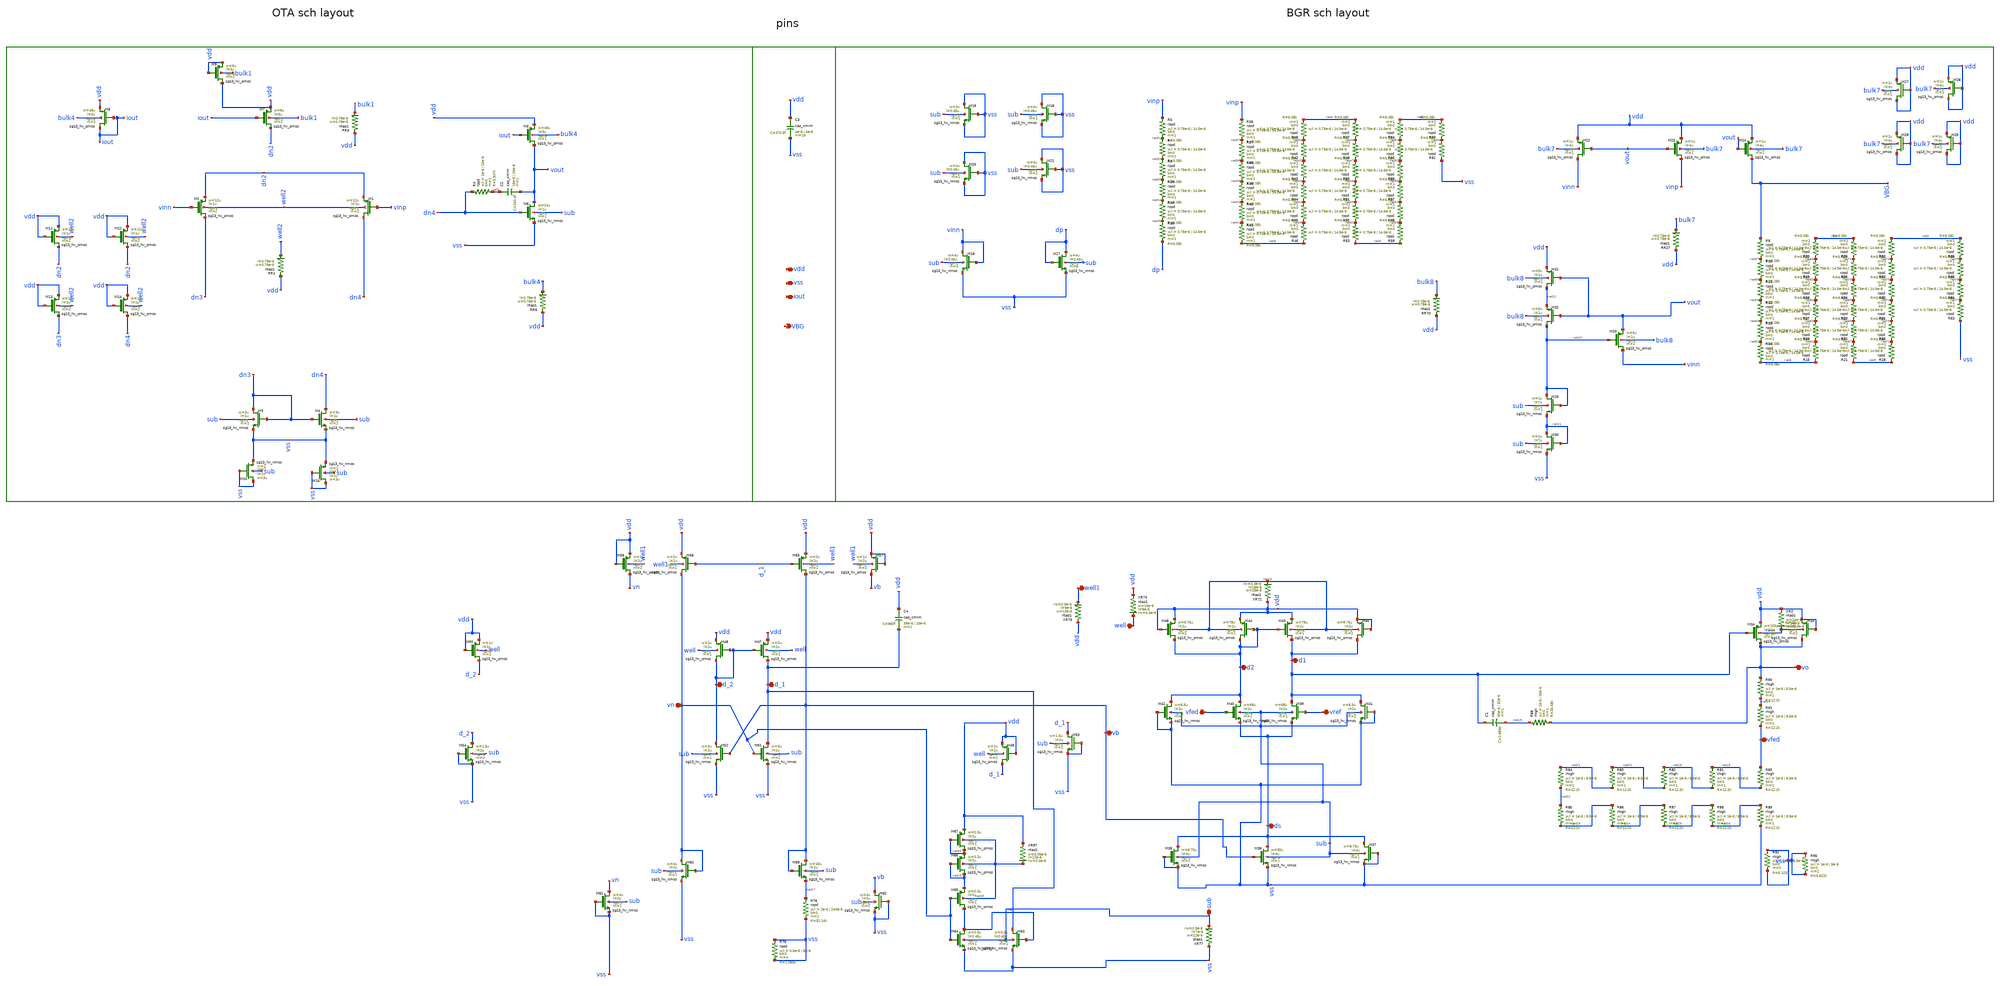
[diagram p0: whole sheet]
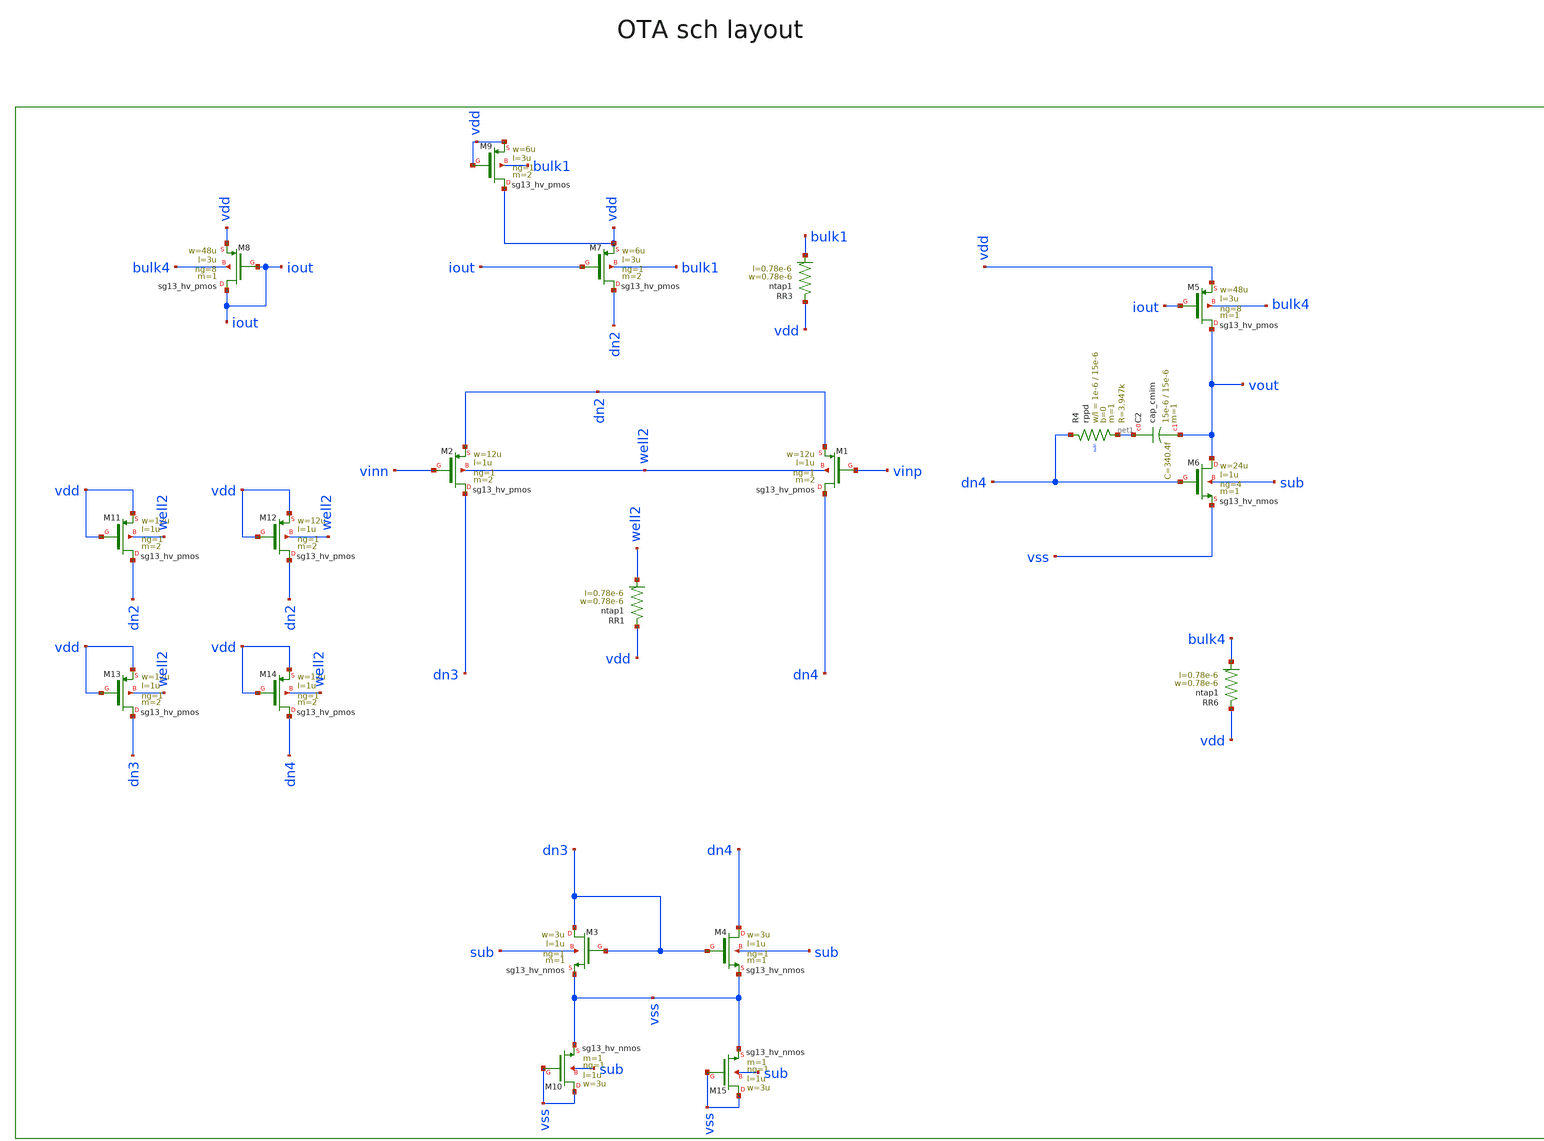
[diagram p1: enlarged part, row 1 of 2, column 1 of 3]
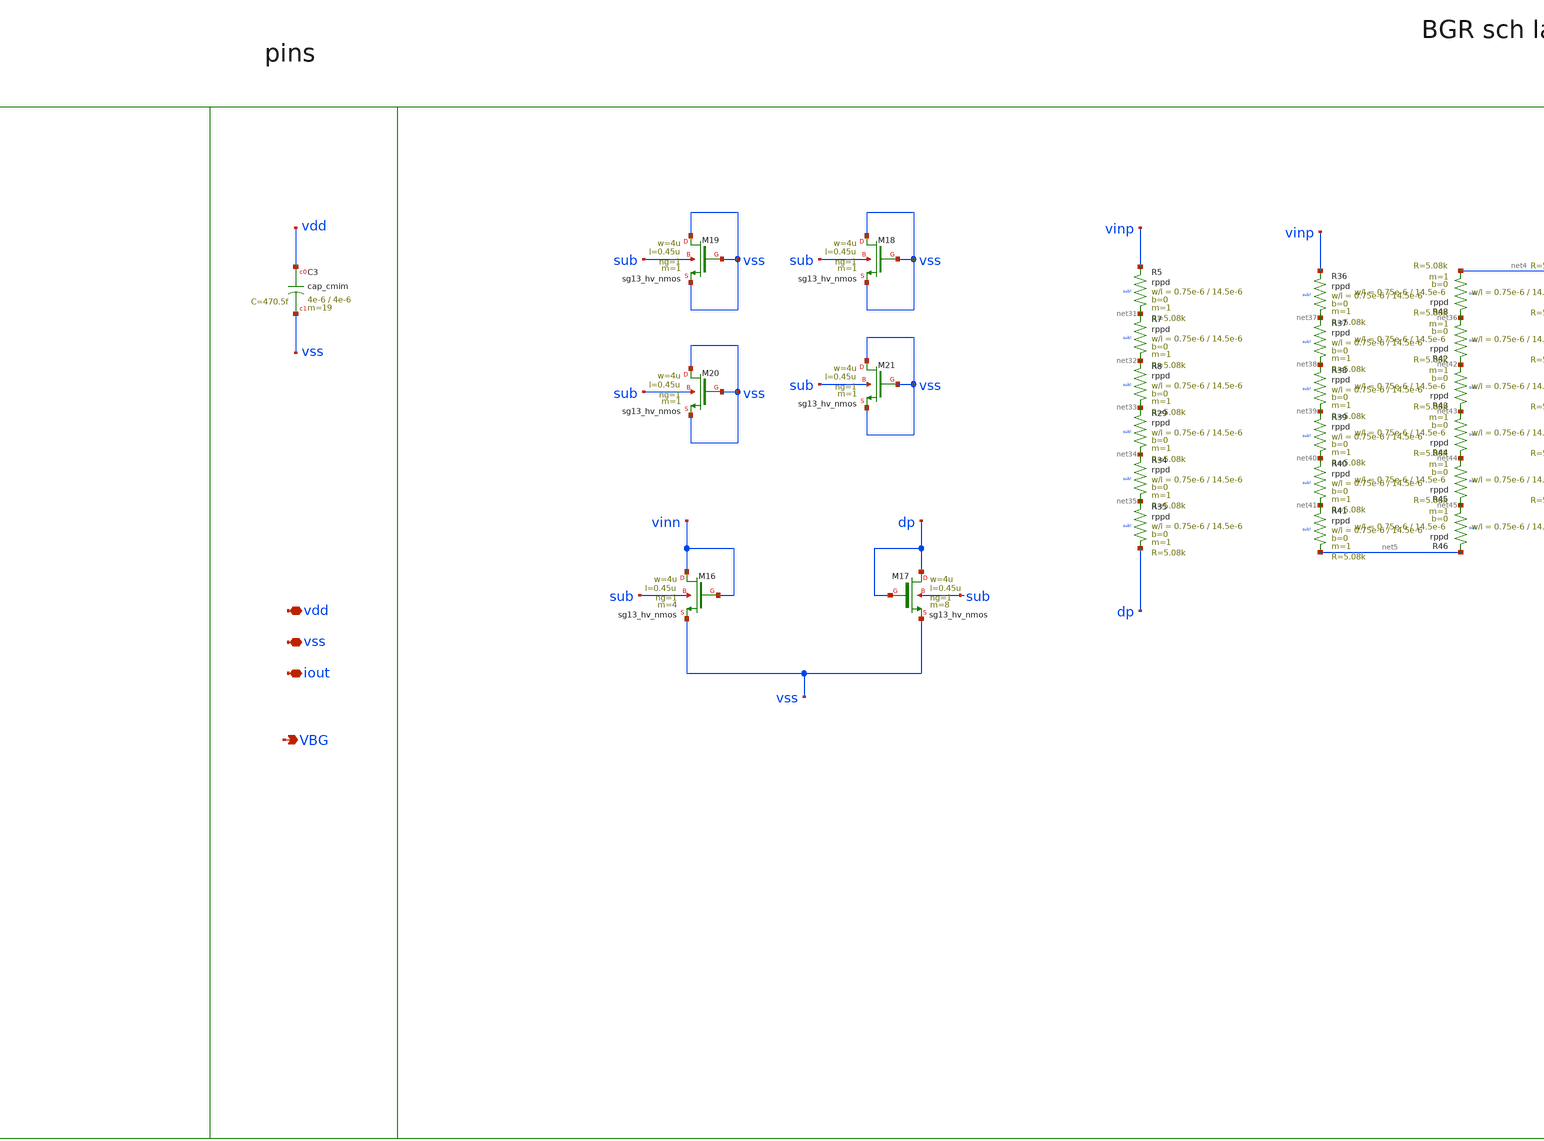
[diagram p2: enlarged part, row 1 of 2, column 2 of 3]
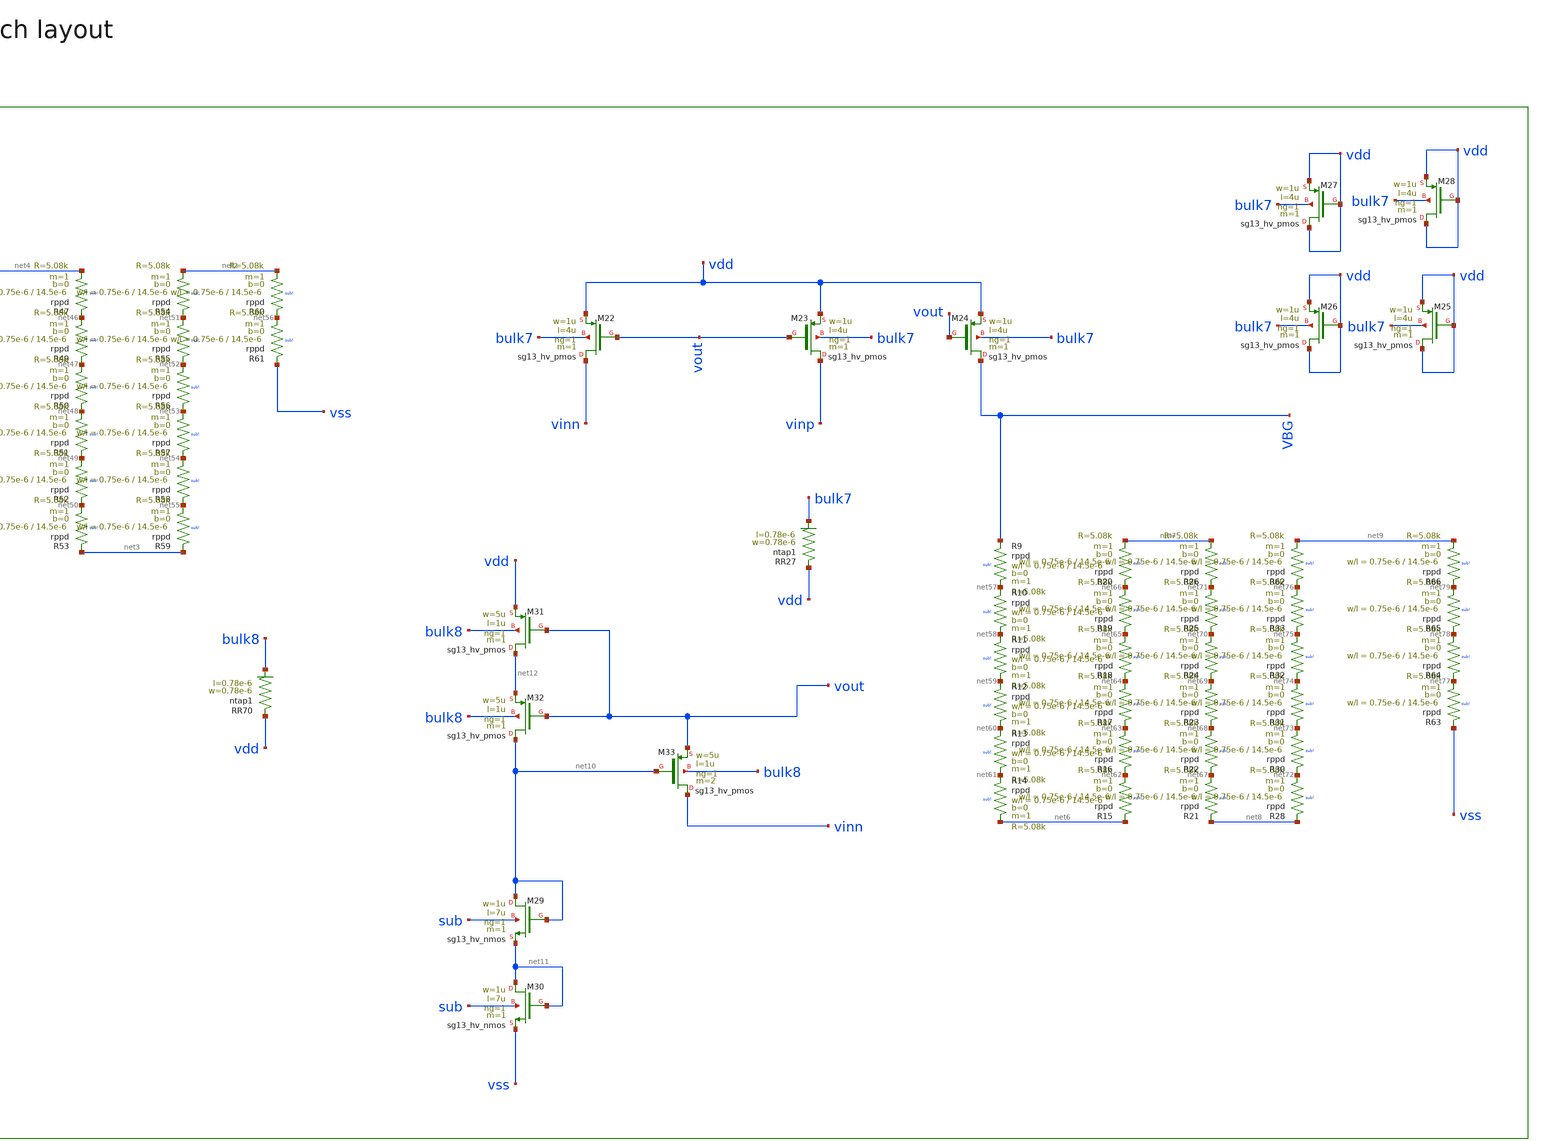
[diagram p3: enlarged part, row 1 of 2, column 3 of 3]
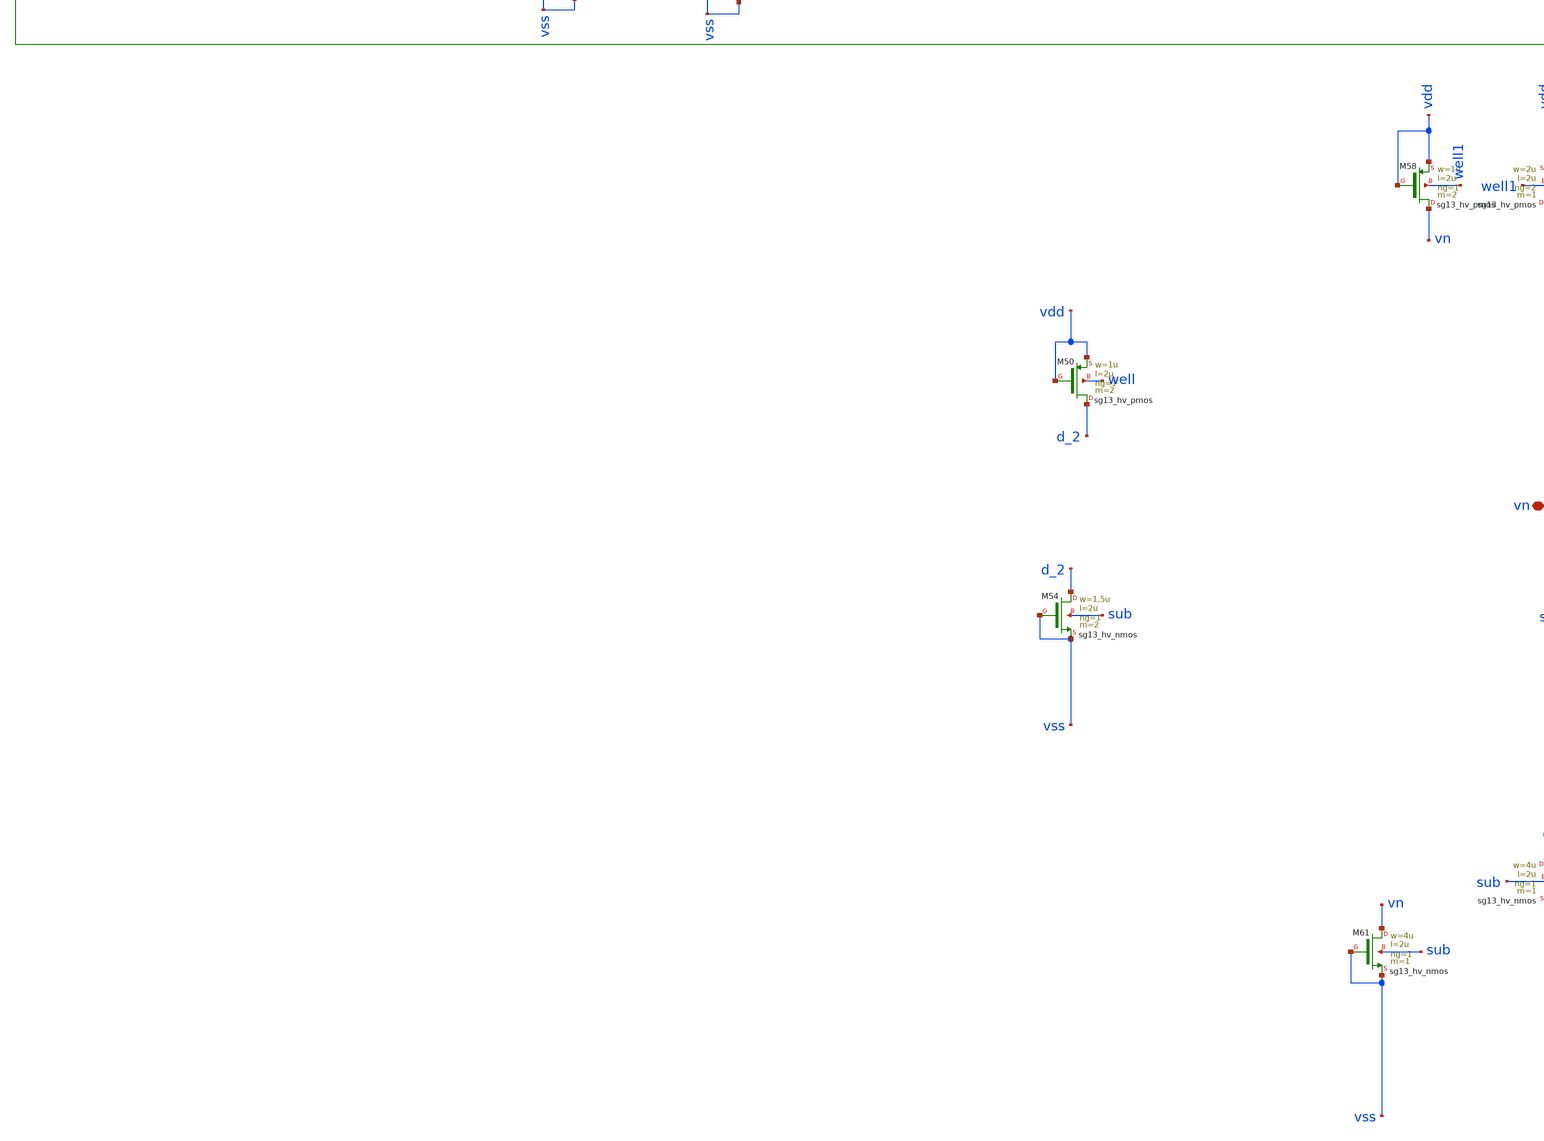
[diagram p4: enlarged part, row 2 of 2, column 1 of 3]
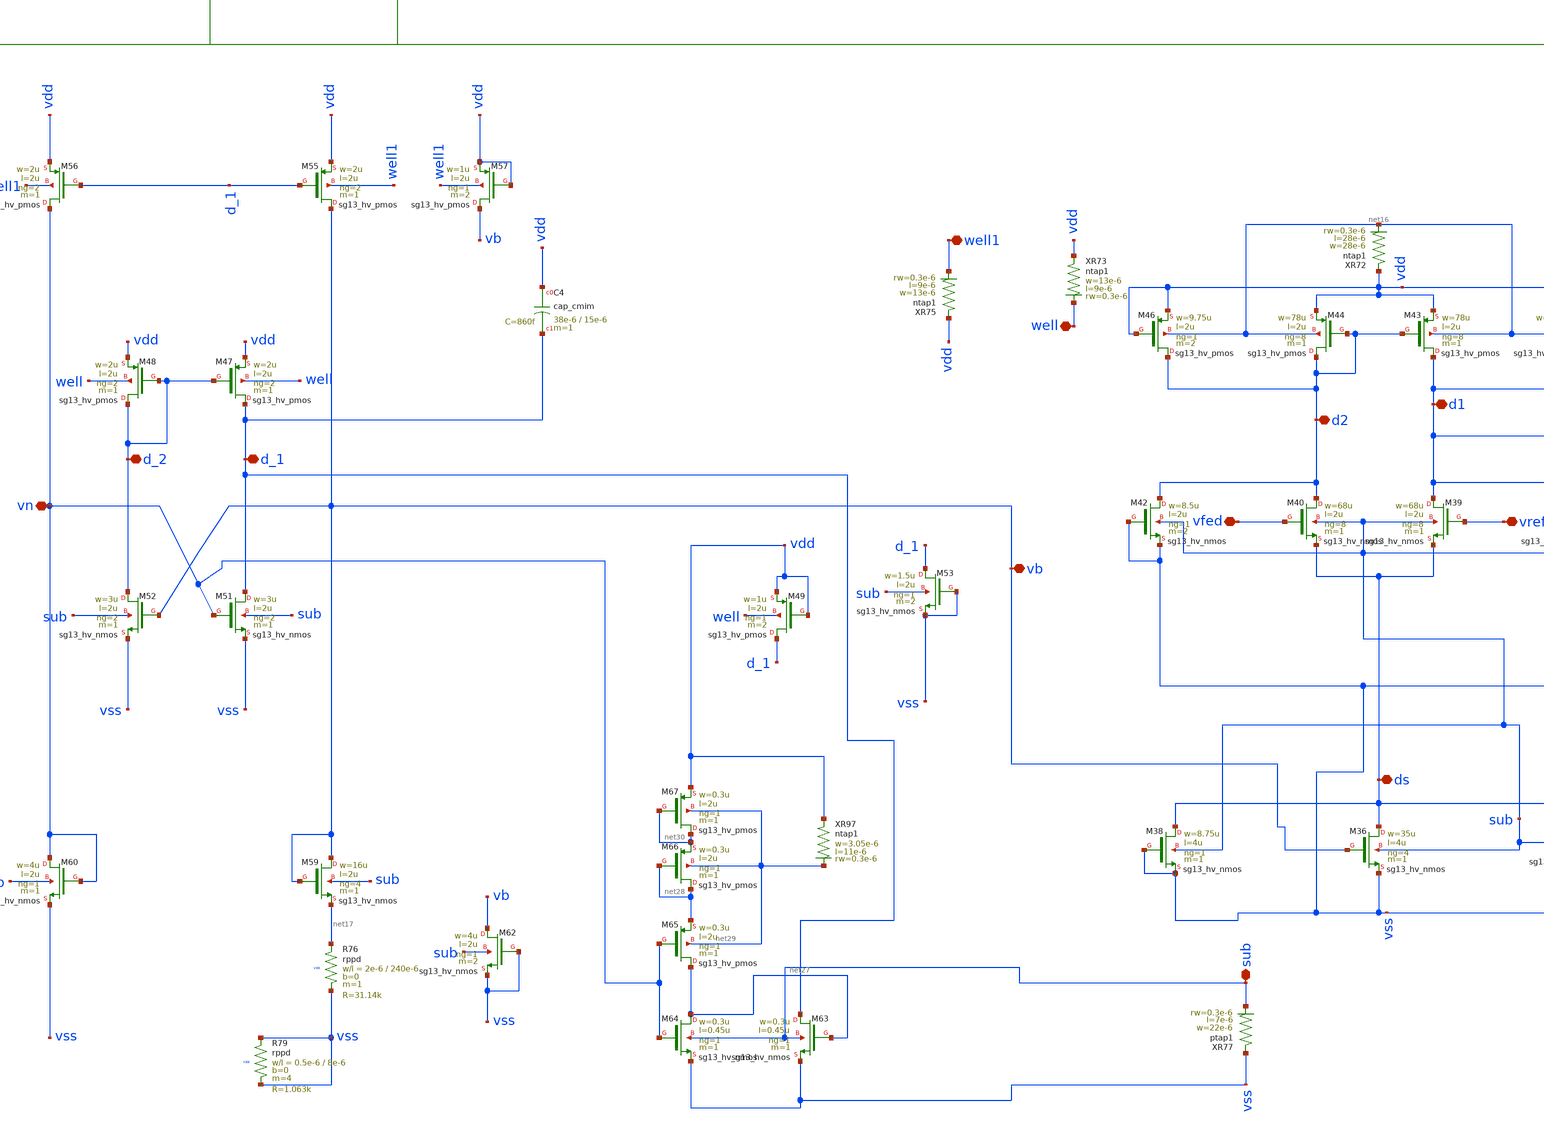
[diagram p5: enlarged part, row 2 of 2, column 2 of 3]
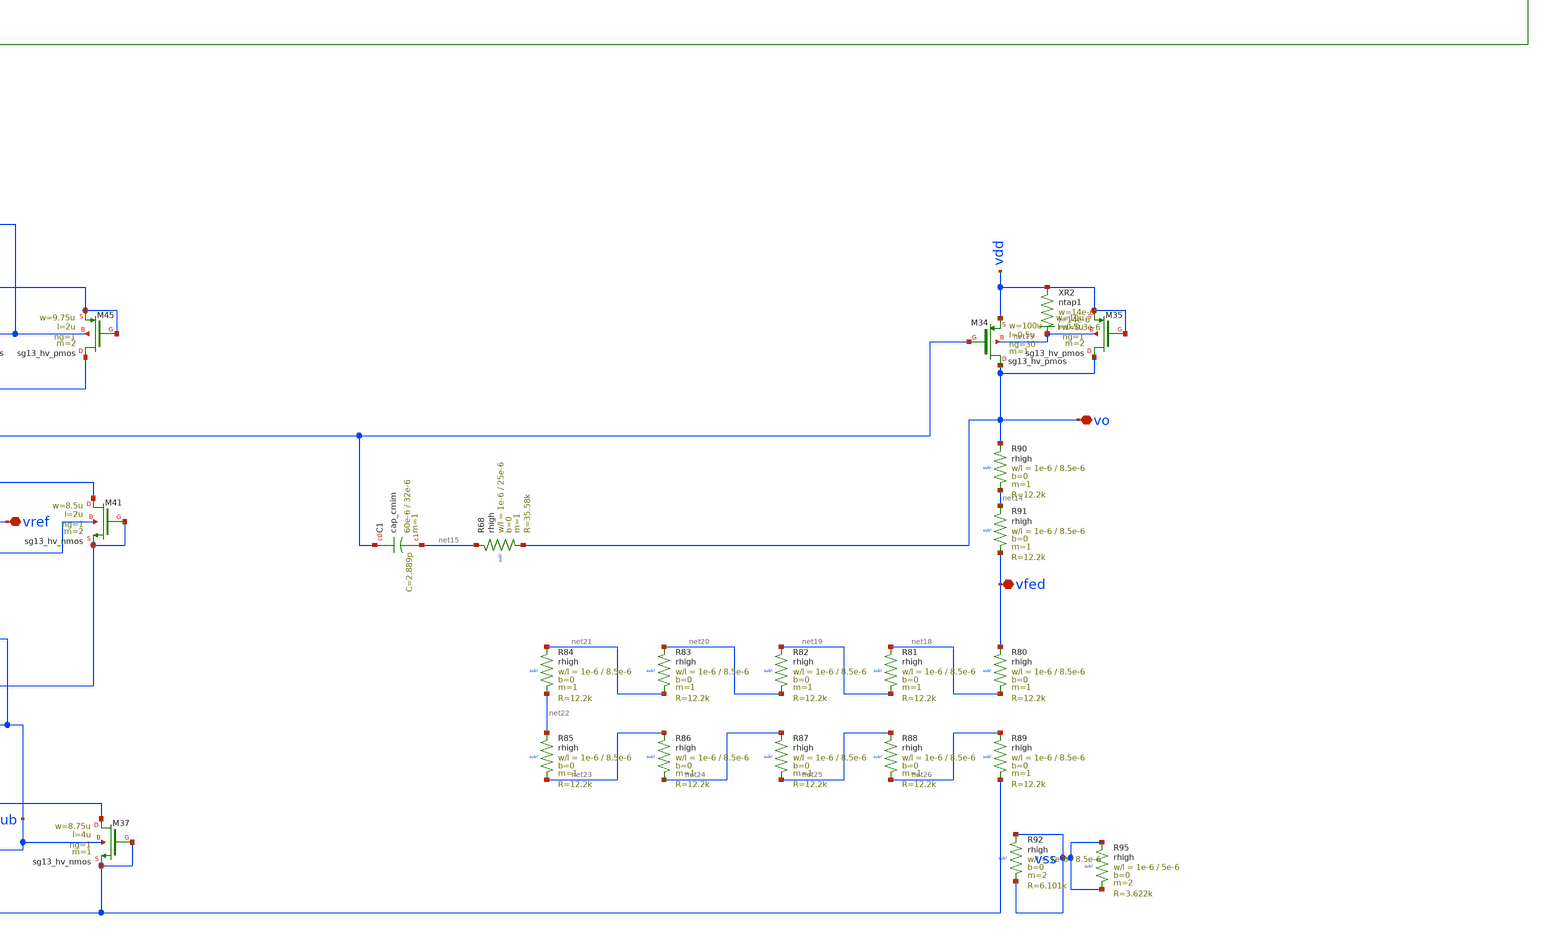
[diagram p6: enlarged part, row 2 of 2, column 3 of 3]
** sch_path: dependencies/pmu_ip/pmu_ip-main/schematic/xschem/pmu_ip.sch
**.subckt pmu_ip vdd vss iout VBG vo vfed ds vref vfed d2 d1 d_2 well vn d_1 well1 sub vb
*.iopin vdd
*.iopin vss
*.iopin iout
*.opin VBG
*.iopin vo
*.iopin vfed
*.iopin ds
*.iopin vref
*.iopin vfed
*.iopin d2
*.iopin d1
*.iopin d_2
*.iopin well
*.iopin vn
*.iopin d_1
*.iopin well1
*.iopin sub
*.iopin vb
XM1 dn4 vinp dn2 well2 sg13_hv_pmos w=12u l=1u ng=1 m=2 mm_ok=1
XM2 dn3 vinn dn2 well2 sg13_hv_pmos w=12u l=1u ng=1 m=2 mm_ok=1
XM11 dn2 vdd vdd well2 sg13_hv_pmos w=12u l=1u ng=1 m=2 mm_ok=1
XM12 dn2 vdd vdd well2 sg13_hv_pmos w=12u l=1u ng=1 m=2 mm_ok=1
XM13 dn3 vdd vdd well2 sg13_hv_pmos w=12u l=1u ng=1 m=2 mm_ok=1
XM14 dn4 vdd vdd well2 sg13_hv_pmos w=12u l=1u ng=1 m=2 mm_ok=1
XR1 vdd well2 ntap1 R=262.8 w=0.78e-6 l=0.78e-6
XR3 vdd bulk1 ntap1 R=262.8 w=0.78e-6 l=0.78e-6
XC2 net1 vout cap_cmim w=15e-6 l=15e-6 m=1 mm_ok=1
XR4 dn4 net1 sub! rppd w=1e-6 l=15e-6 m=1 b=0 mm_ok=1
XR6 vdd bulk4 ntap1 R=262.8 w=0.78e-6 l=0.78e-6
XM5 vout iout vdd bulk4 sg13_hv_pmos w=48u l=3u ng=8 m=1 mm_ok=1
XM6 vout dn4 vss sub sg13_hv_nmos w=24u l=1u ng=4 m=1 mm_ok=1
XM7 dn2 iout vdd bulk1 sg13_hv_pmos w=6u l=3u ng=1 m=2 mm_ok=1
XM8 iout iout vdd bulk4 sg13_hv_pmos w=48u l=3u ng=8 m=1 mm_ok=1
XM3 dn3 dn3 vss sub sg13_hv_nmos w=3u l=1u ng=1 m=1 mm_ok=1
XM4 dn4 dn3 vss sub sg13_hv_nmos w=3u l=1u ng=1 m=1 mm_ok=1
XM9 vdd vdd vdd bulk1 sg13_hv_pmos w=6u l=3u ng=1 m=2 mm_ok=1
XM10 vss vss vss sub sg13_hv_nmos w=3u l=1u ng=1 m=1 mm_ok=1
XM15 vss vss vss sub sg13_hv_nmos w=3u l=1u ng=1 m=1 mm_ok=1
XM16 vinn vinn vss sub sg13_hv_nmos w=4u l=0.45u ng=1 m=4 mm_ok=1
XM17 dp dp vss sub sg13_hv_nmos w=4u l=0.45u ng=1 m=8 mm_ok=1
XM18 vss vss vss sub sg13_hv_nmos w=4u l=0.45u ng=1 m=1 mm_ok=1
XM19 vss vss vss sub sg13_hv_nmos w=4u l=0.45u ng=1 m=1 mm_ok=1
XM20 vss vss vss sub sg13_hv_nmos w=4u l=0.45u ng=1 m=1 mm_ok=1
XM21 vss vss vss sub sg13_hv_nmos w=4u l=0.45u ng=1 m=1 mm_ok=1
XR5 vinp net31 sub! rppd w=0.75e-6 l=14.5e-6 m=1 b=0 mm_ok=1
XR7 net31 net32 sub! rppd w=0.75e-6 l=14.5e-6 m=1 b=0 mm_ok=1
XR8 net32 net33 sub! rppd w=0.75e-6 l=14.5e-6 m=1 b=0 mm_ok=1
XR29 net33 net34 sub! rppd w=0.75e-6 l=14.5e-6 m=1 b=0 mm_ok=1
XR34 net34 net35 sub! rppd w=0.75e-6 l=14.5e-6 m=1 b=0 mm_ok=1
XR35 net35 dp sub! rppd w=0.75e-6 l=14.5e-6 m=1 b=0 mm_ok=1
XR48 net36 net4 sub! rppd w=0.75e-6 l=14.5e-6 m=1 b=0 mm_ok=1
XR36 vinp net37 sub! rppd w=0.75e-6 l=14.5e-6 m=1 b=0 mm_ok=1
XR37 net37 net38 sub! rppd w=0.75e-6 l=14.5e-6 m=1 b=0 mm_ok=1
XR38 net38 net39 sub! rppd w=0.75e-6 l=14.5e-6 m=1 b=0 mm_ok=1
XR39 net39 net40 sub! rppd w=0.75e-6 l=14.5e-6 m=1 b=0 mm_ok=1
XR40 net40 net41 sub! rppd w=0.75e-6 l=14.5e-6 m=1 b=0 mm_ok=1
XR41 net41 net5 sub! rppd w=0.75e-6 l=14.5e-6 m=1 b=0 mm_ok=1
XR42 net42 net36 sub! rppd w=0.75e-6 l=14.5e-6 m=1 b=0 mm_ok=1
XR43 net43 net42 sub! rppd w=0.75e-6 l=14.5e-6 m=1 b=0 mm_ok=1
XR44 net44 net43 sub! rppd w=0.75e-6 l=14.5e-6 m=1 b=0 mm_ok=1
XR45 net45 net44 sub! rppd w=0.75e-6 l=14.5e-6 m=1 b=0 mm_ok=1
XR46 net5 net45 sub! rppd w=0.75e-6 l=14.5e-6 m=1 b=0 mm_ok=1
XR47 net46 net4 sub! rppd w=0.75e-6 l=14.5e-6 m=1 b=0 mm_ok=1
XR49 net47 net46 sub! rppd w=0.75e-6 l=14.5e-6 m=1 b=0 mm_ok=1
XR50 net48 net47 sub! rppd w=0.75e-6 l=14.5e-6 m=1 b=0 mm_ok=1
XR51 net49 net48 sub! rppd w=0.75e-6 l=14.5e-6 m=1 b=0 mm_ok=1
XR52 net50 net49 sub! rppd w=0.75e-6 l=14.5e-6 m=1 b=0 mm_ok=1
XR53 net3 net50 sub! rppd w=0.75e-6 l=14.5e-6 m=1 b=0 mm_ok=1
XR54 net51 net2 sub! rppd w=0.75e-6 l=14.5e-6 m=1 b=0 mm_ok=1
XR55 net52 net51 sub! rppd w=0.75e-6 l=14.5e-6 m=1 b=0 mm_ok=1
XR56 net53 net52 sub! rppd w=0.75e-6 l=14.5e-6 m=1 b=0 mm_ok=1
XR57 net54 net53 sub! rppd w=0.75e-6 l=14.5e-6 m=1 b=0 mm_ok=1
XR58 net55 net54 sub! rppd w=0.75e-6 l=14.5e-6 m=1 b=0 mm_ok=1
XR59 net3 net55 sub! rppd w=0.75e-6 l=14.5e-6 m=1 b=0 mm_ok=1
XR60 net56 net2 sub! rppd w=0.75e-6 l=14.5e-6 m=1 b=0 mm_ok=1
XR61 vss net56 sub! rppd w=0.75e-6 l=14.5e-6 m=1 b=0 mm_ok=1
XM22 vinn vout vdd bulk7 sg13_hv_pmos w=1u l=4u ng=1 m=1 mm_ok=1
XM23 vinp vout vdd bulk7 sg13_hv_pmos w=1u l=4u ng=1 m=1 mm_ok=1
XM24 VBG vout vdd bulk7 sg13_hv_pmos w=1u l=4u ng=1 m=1 mm_ok=1
XR27 vdd bulk7 ntap1 R=262.8 w=0.78e-6 l=0.78e-6
XR9 VBG net57 sub! rppd w=0.75e-6 l=14.5e-6 m=1 b=0 mm_ok=1
XR10 net57 net58 sub! rppd w=0.75e-6 l=14.5e-6 m=1 b=0 mm_ok=1
XR11 net58 net59 sub! rppd w=0.75e-6 l=14.5e-6 m=1 b=0 mm_ok=1
XR12 net59 net60 sub! rppd w=0.75e-6 l=14.5e-6 m=1 b=0 mm_ok=1
XR13 net60 net61 sub! rppd w=0.75e-6 l=14.5e-6 m=1 b=0 mm_ok=1
XR14 net61 net6 sub! rppd w=0.75e-6 l=14.5e-6 m=1 b=0 mm_ok=1
XR15 net6 net62 sub! rppd w=0.75e-6 l=14.5e-6 m=1 b=0 mm_ok=1
XR16 net62 net63 sub! rppd w=0.75e-6 l=14.5e-6 m=1 b=0 mm_ok=1
XR17 net63 net64 sub! rppd w=0.75e-6 l=14.5e-6 m=1 b=0 mm_ok=1
XR18 net64 net65 sub! rppd w=0.75e-6 l=14.5e-6 m=1 b=0 mm_ok=1
XR19 net65 net66 sub! rppd w=0.75e-6 l=14.5e-6 m=1 b=0 mm_ok=1
XR20 net66 net7 sub! rppd w=0.75e-6 l=14.5e-6 m=1 b=0 mm_ok=1
XR21 net8 net67 sub! rppd w=0.75e-6 l=14.5e-6 m=1 b=0 mm_ok=1
XR22 net67 net68 sub! rppd w=0.75e-6 l=14.5e-6 m=1 b=0 mm_ok=1
XR23 net68 net69 sub! rppd w=0.75e-6 l=14.5e-6 m=1 b=0 mm_ok=1
XR24 net69 net70 sub! rppd w=0.75e-6 l=14.5e-6 m=1 b=0 mm_ok=1
XR25 net70 net71 sub! rppd w=0.75e-6 l=14.5e-6 m=1 b=0 mm_ok=1
XR26 net71 net7 sub! rppd w=0.75e-6 l=14.5e-6 m=1 b=0 mm_ok=1
XR28 net8 net72 sub! rppd w=0.75e-6 l=14.5e-6 m=1 b=0 mm_ok=1
XR30 net72 net73 sub! rppd w=0.75e-6 l=14.5e-6 m=1 b=0 mm_ok=1
XR31 net73 net74 sub! rppd w=0.75e-6 l=14.5e-6 m=1 b=0 mm_ok=1
XR32 net74 net75 sub! rppd w=0.75e-6 l=14.5e-6 m=1 b=0 mm_ok=1
XR33 net75 net76 sub! rppd w=0.75e-6 l=14.5e-6 m=1 b=0 mm_ok=1
XR62 net76 net9 sub! rppd w=0.75e-6 l=14.5e-6 m=1 b=0 mm_ok=1
XR63 vss net77 sub! rppd w=0.75e-6 l=14.5e-6 m=1 b=0 mm_ok=1
XR64 net77 net78 sub! rppd w=0.75e-6 l=14.5e-6 m=1 b=0 mm_ok=1
XR65 net78 net79 sub! rppd w=0.75e-6 l=14.5e-6 m=1 b=0 mm_ok=1
XR66 net79 net9 sub! rppd w=0.75e-6 l=14.5e-6 m=1 b=0 mm_ok=1
XM25 vdd vdd vdd bulk7 sg13_hv_pmos w=1u l=4u ng=1 m=1 mm_ok=1
XM26 vdd vdd vdd bulk7 sg13_hv_pmos w=1u l=4u ng=1 m=1 mm_ok=1
XM27 vdd vdd vdd bulk7 sg13_hv_pmos w=1u l=4u ng=1 m=1 mm_ok=1
XM28 vdd vdd vdd bulk7 sg13_hv_pmos w=1u l=4u ng=1 m=1 mm_ok=1
XM29 net10 net10 net11 sub sg13_hv_nmos w=1u l=7u ng=1 m=1 mm_ok=1
XM30 net11 net11 vss sub sg13_hv_nmos w=1u l=7u ng=1 m=1 mm_ok=1
XM31 net12 vout vdd bulk8 sg13_hv_pmos w=5u l=1u ng=1 m=1 mm_ok=1
XM32 net10 vout net12 bulk8 sg13_hv_pmos w=5u l=1u ng=1 m=1 mm_ok=1
XM33 vinn net10 vout bulk8 sg13_hv_pmos w=5u l=1u ng=1 m=2 mm_ok=1
XR70 vdd bulk8 ntap1 R=262.8 w=0.78e-6 l=0.78e-6
XC3 vdd vss cap_cmim w=4e-6 l=4e-6 m=19 mm_ok=1
XM34 vo d1 vdd net13 sg13_hv_pmos w=100u l=0.5u ng=30 m=1 mm_ok=1
XM35 vo vdd vdd net13 sg13_hv_pmos w=10u l=0.5u ng=1 m=2 mm_ok=1
XR2 vdd net13 ntap1 R=4.159 w=14e-6 l=14e-6 rw=0.3e-6
XC1 d1 net15 cap_cmim w=60e-6 l=32e-6 m=1 mm_ok=1
XR68 net15 vo sub! rhigh w=1e-6 l=25e-6 m=1 b=0 mm_ok=1
XM36 ds vb vss sub sg13_hv_nmos w=35u l=4u ng=4 m=1 mm_ok=1
XM37 ds vss vss sub sg13_hv_nmos w=8.75u l=4u ng=1 m=1 mm_ok=1
XM38 ds vss vss sub sg13_hv_nmos w=8.75u l=4u ng=1 m=1 mm_ok=1
XM39 d1 vref ds sub sg13_hv_nmos w=68u l=2u ng=8 m=1 mm_ok=1
XM40 d2 vfed ds sub sg13_hv_nmos w=68u l=2u ng=8 m=1 mm_ok=1
XM41 d1 vss vss sub sg13_hv_nmos w=8.5u l=2u ng=1 m=2 mm_ok=1
XM42 d2 vss vss sub sg13_hv_nmos w=8.5u l=2u ng=1 m=2 mm_ok=1
XM43 d1 d2 vdd net16 sg13_hv_pmos w=78u l=2u ng=8 m=1 mm_ok=1
XM44 d2 d2 vdd net16 sg13_hv_pmos w=78u l=2u ng=8 m=1 mm_ok=1
XM45 d1 vdd vdd net16 sg13_hv_pmos w=9.75u l=2u ng=1 m=2 mm_ok=1
XM46 d2 vdd vdd net16 sg13_hv_pmos w=9.75u l=2u ng=1 m=2 mm_ok=1
XR72 vdd net16 ntap1 R=2.057 w=28e-6 l=28e-6 rw=0.3e-6
XM47 d_1 d_2 vdd well sg13_hv_pmos w=2u l=2u ng=2 m=1 mm_ok=1
XM48 d_2 d_2 vdd well sg13_hv_pmos w=2u l=2u ng=2 m=1 mm_ok=1
XR73 vdd well ntap1 R=5.325 w=13e-6 l=9e-6 rw=0.3e-6
XM49 d_1 vdd vdd well sg13_hv_pmos w=1u l=2u ng=1 m=2 mm_ok=1
XM50 d_2 vdd vdd well sg13_hv_pmos w=1u l=2u ng=1 m=2 mm_ok=1
XM51 d_1 vn vss sub sg13_hv_nmos w=3u l=2u ng=2 m=1 mm_ok=1
XM52 d_2 vb vss sub sg13_hv_nmos w=3u l=2u ng=2 m=1 mm_ok=1
XM53 d_1 vss vss sub sg13_hv_nmos w=1.5u l=2u ng=1 m=2 mm_ok=1
XM54 d_2 vss vss sub sg13_hv_nmos w=1.5u l=2u ng=1 m=2 mm_ok=1
XM55 vb d_1 vdd well1 sg13_hv_pmos w=2u l=2u ng=2 m=1 mm_ok=1
XM56 vn d_1 vdd well1 sg13_hv_pmos w=2u l=2u ng=2 m=1 mm_ok=1
XR75 vdd well1 ntap1 R=5.325 w=13e-6 l=9e-6 rw=0.3e-6
XM57 vb vdd vdd well1 sg13_hv_pmos w=1u l=2u ng=1 m=2 mm_ok=1
XM58 vn vdd vdd well1 sg13_hv_pmos w=1u l=2u ng=1 m=2 mm_ok=1
XM59 vb vb net17 sub sg13_hv_nmos w=16u l=2u ng=4 m=1 mm_ok=1
XM60 vn vn vss sub sg13_hv_nmos w=4u l=2u ng=1 m=1 mm_ok=1
XR76 net17 vss vss rppd w=2e-6 l=240e-6 m=1 b=0 mm_ok=1
XR77 vss sub ptap1 R=4.012 w=22e-6 l=7e-6 rw=0.3e-6
XM61 vn vss vss sub sg13_hv_nmos w=4u l=2u ng=1 m=1 mm_ok=1
XM62 vb vss vss sub sg13_hv_nmos w=4u l=2u ng=1 m=2 mm_ok=1
XC4 vdd d_1 cap_cmim w=38e-6 l=15e-6 m=1 mm_ok=1
XR79 vss vss vss rppd w=0.5e-6 l=8e-6 m=4 b=0 mm_ok=1
XR80 vfed net18 sub! rhigh w=1e-6 l=8.5e-6 m=1 b=0 mm_ok=1
XR81 net18 net19 sub! rhigh w=1e-6 l=8.5e-6 m=1 b=0 mm_ok=1
XR82 net19 net20 sub! rhigh w=1e-6 l=8.5e-6 m=1 b=0 mm_ok=1
XR83 net20 net21 sub! rhigh w=1e-6 l=8.5e-6 m=1 b=0 mm_ok=1
XR84 net21 net22 sub! rhigh w=1e-6 l=8.5e-6 m=1 b=0 mm_ok=1
XR85 net22 net23 sub! rhigh w=1e-6 l=8.5e-6 m=1 b=0 mm_ok=1
XR86 net23 net24 sub! rhigh w=1e-6 l=8.5e-6 m=1 b=0 mm_ok=1
XR87 net24 net25 sub! rhigh w=1e-6 l=8.5e-6 m=1 b=0 mm_ok=1
XR88 net25 net26 sub! rhigh w=1e-6 l=8.5e-6 m=1 b=0 mm_ok=1
XR89 net26 vss sub! rhigh w=1e-6 l=8.5e-6 m=1 b=0 mm_ok=1
XR90 vo net14 sub! rhigh w=1e-6 l=8.5e-6 m=1 b=0 mm_ok=1
XR91 net14 vfed sub! rhigh w=1e-6 l=8.5e-6 m=1 b=0 mm_ok=1
XR92 vss vss sub! rhigh w=1e-6 l=8.5e-6 m=2 b=0 mm_ok=1
XR95 vss vss sub! rhigh w=1e-6 l=5e-6 m=2 b=0 mm_ok=1
XM63 d_1 net27 vss sub sg13_hv_nmos w=0.3u l=0.45u ng=1 m=1 mm_ok=1
XM64 net27 vn vss sub sg13_hv_nmos w=0.3u l=0.45u ng=1 m=1 mm_ok=1
XM65 net27 vn net28 net29 sg13_hv_pmos w=0.3u l=2u ng=1 m=1 mm_ok=1
XM66 net28 net28 net30 net29 sg13_hv_pmos w=0.3u l=2u ng=1 m=1 mm_ok=1
XM67 net30 net30 vdd net29 sg13_hv_pmos w=0.3u l=2u ng=1 m=1 mm_ok=1
XR97 vdd net29 ntap1 R=8.472 w=3.05e-6 l=11e-6 rw=0.3e-6
**.ends
.end
